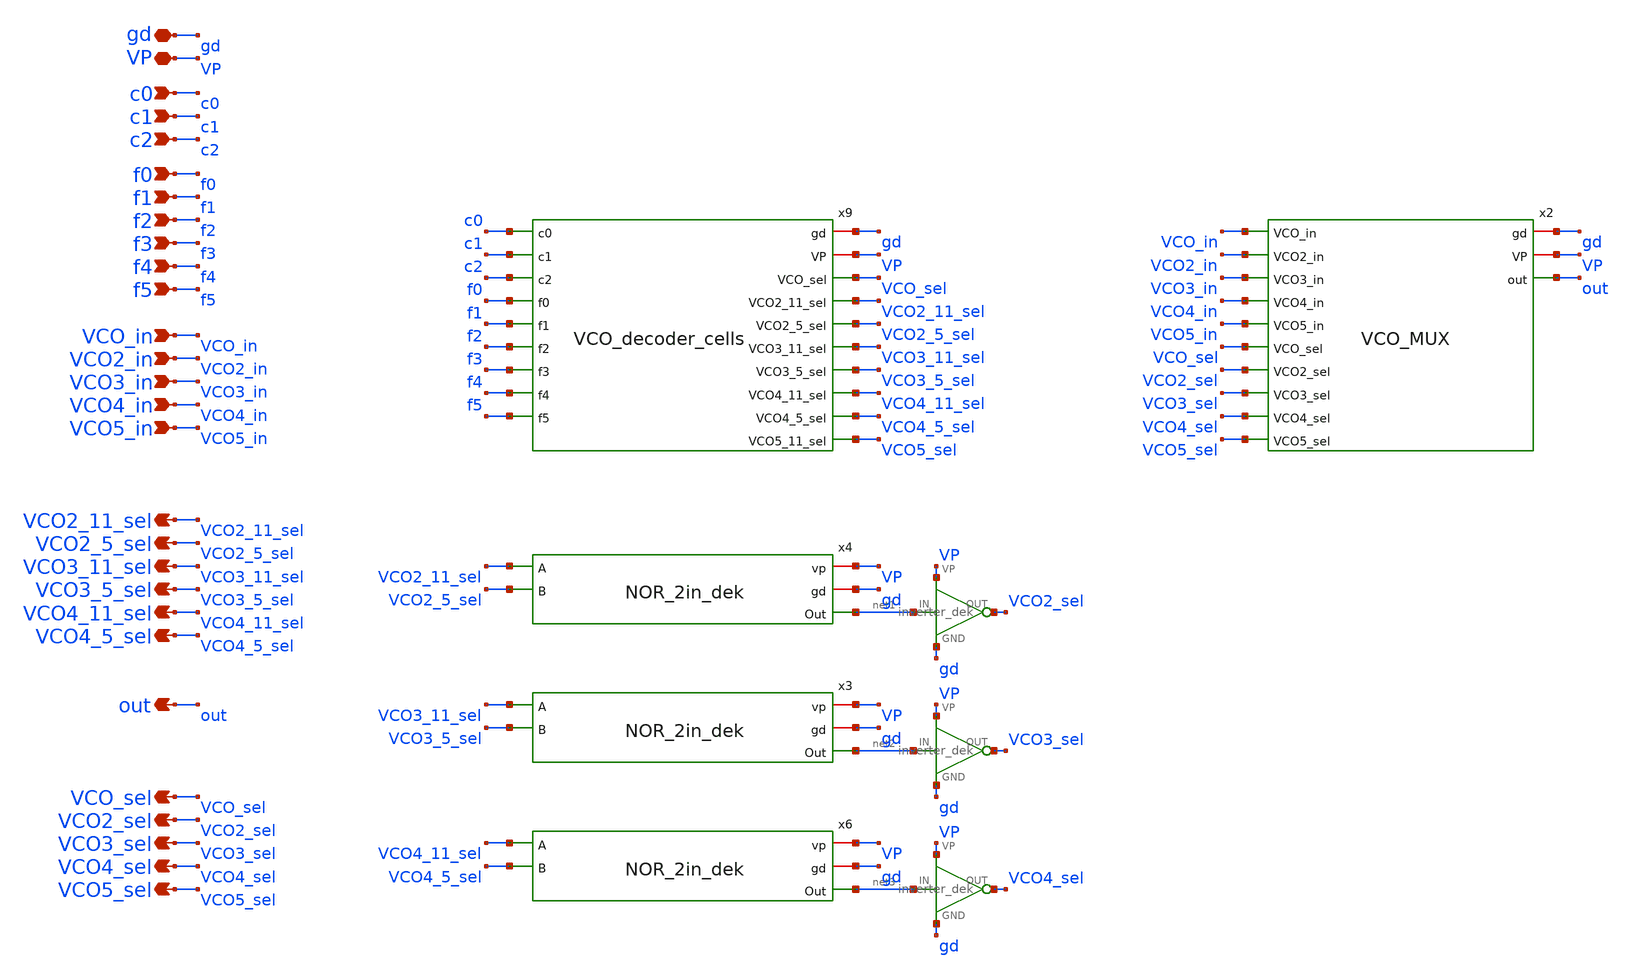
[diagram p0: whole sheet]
** sch_path: schematics/divider/schematics/VCO_MUX_and_decoder.sch
**.subckt VCO_MUX_and_decoder gd VP c1 c2 f0 f1 c0 VCO2_11_sel VCO2_5_sel VCO3_11_sel VCO3_5_sel
*+ VCO4_11_sel VCO4_5_sel f2 f3 f4 f5 VCO_in VCO2_in VCO3_in VCO4_in VCO5_in out VCO_sel VCO2_sel VCO3_sel
*+ VCO4_sel VCO5_sel
*.iopin gd
*.iopin VP
*.ipin c1
*.ipin c2
*.ipin f0
*.ipin f1
*.ipin c0
*.opin VCO2_11_sel
*.opin VCO2_5_sel
*.opin VCO3_11_sel
*.opin VCO3_5_sel
*.opin VCO4_11_sel
*.opin VCO4_5_sel
*.ipin f2
*.ipin f3
*.ipin f4
*.ipin f5
*.ipin VCO_in
*.ipin VCO2_in
*.ipin VCO3_in
*.ipin VCO4_in
*.ipin VCO5_in
*.opin out
*.opin VCO_sel
*.opin VCO2_sel
*.opin VCO3_sel
*.opin VCO4_sel
*.opin VCO5_sel
x2 gd VP VCO_in VCO2_in VCO3_in VCO4_in VCO5_in VCO_sel VCO2_sel VCO3_sel VCO4_sel VCO5_sel out
+ VCO_MUX
x4 VP gd VCO2_11_sel net1 VCO2_5_sel NOR_2in_dek
x5 net1 VCO2_sel VP gd inverter_dek
x3 VP gd VCO3_11_sel net2 VCO3_5_sel NOR_2in_dek
x6 VP gd VCO4_11_sel net3 VCO4_5_sel NOR_2in_dek
x7 net2 VCO3_sel VP gd inverter_dek
x8 net3 VCO4_sel VP gd inverter_dek
x9 gd VP c0 c1 c2 f0 f1 f2 f3 f4 f5 VCO_sel VCO2_11_sel VCO2_5_sel VCO3_11_sel VCO3_5_sel
+ VCO4_11_sel VCO4_5_sel VCO5_sel VCO_decoder_cells
**.ends
.end
